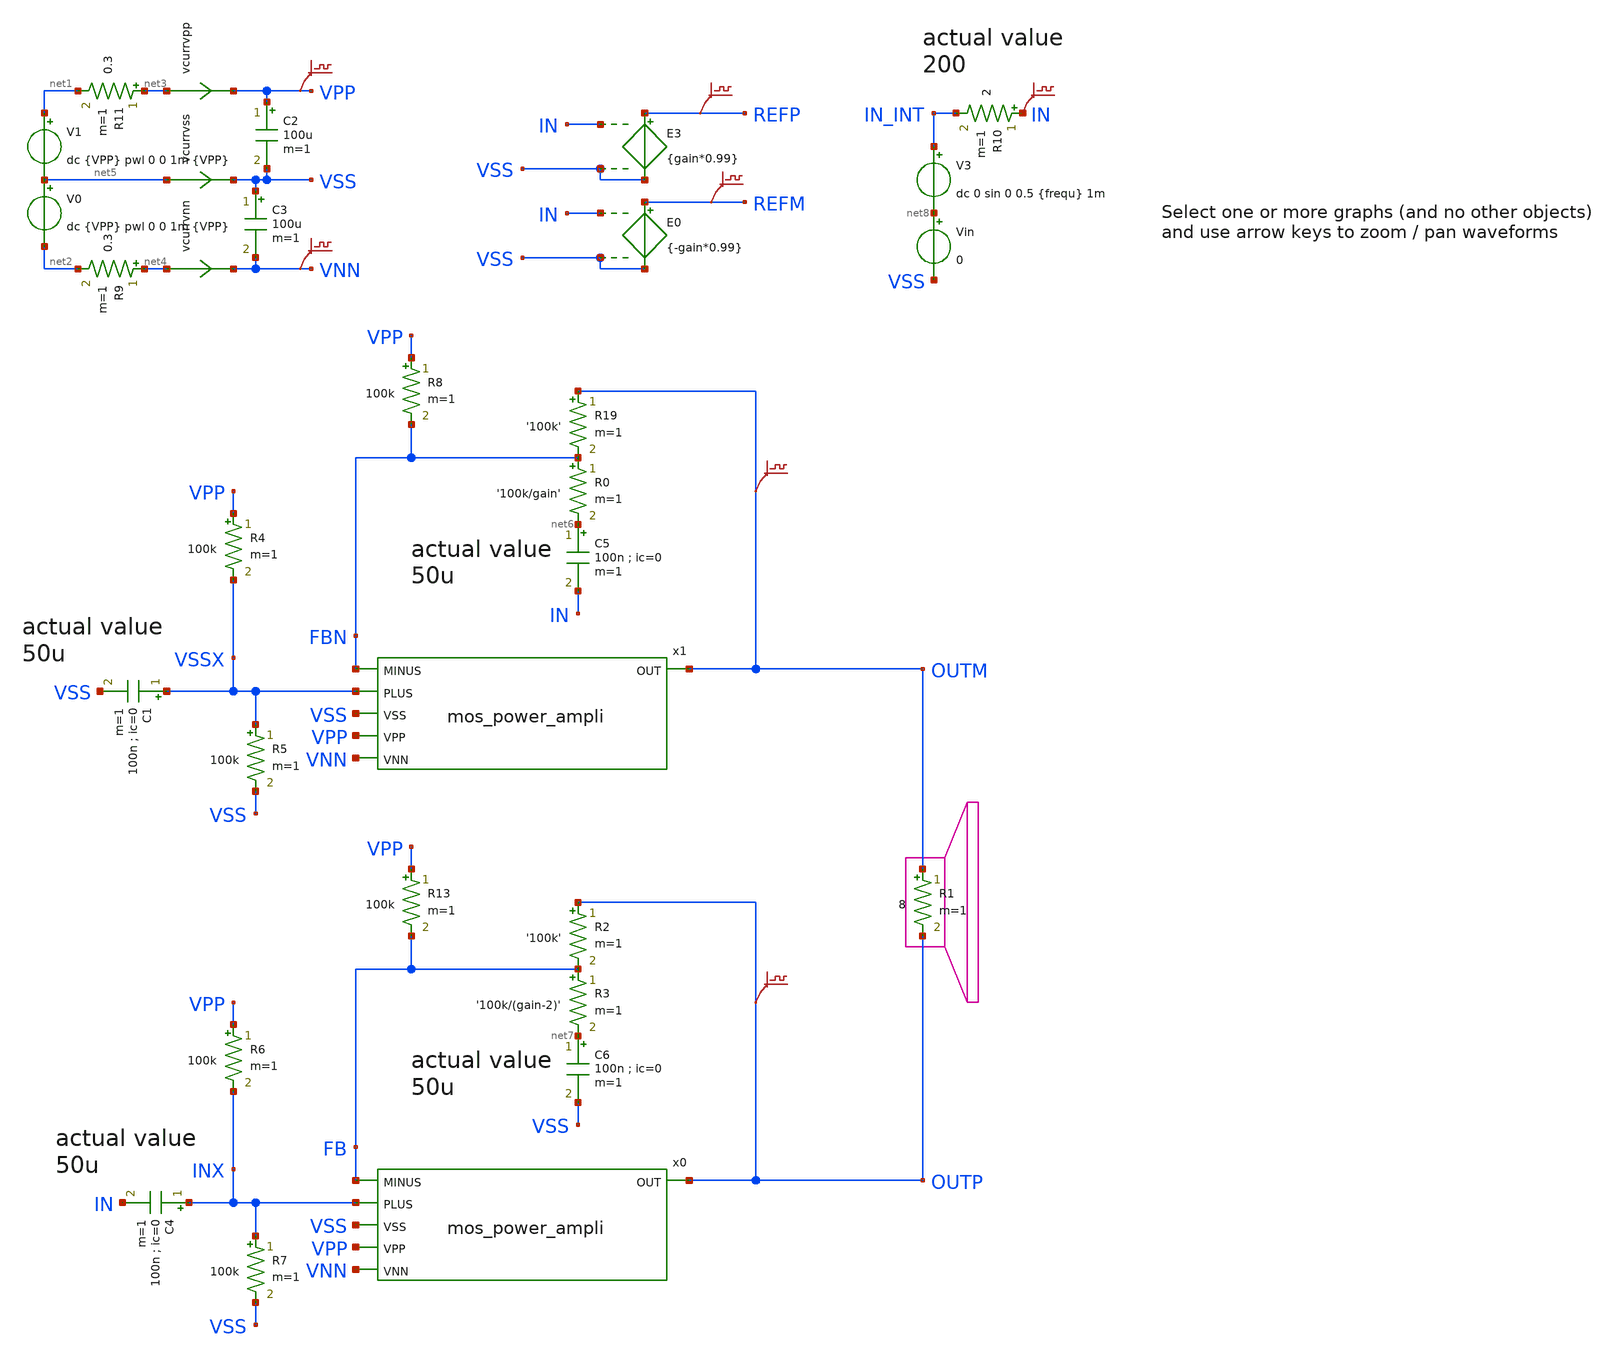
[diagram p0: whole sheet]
** sch_path: xschem_library/examples/poweramp.sch
* Copyright (C) 1998-2023 Stefan Frederik Schippers
* This program is free software; you can redistribute it and/or modify
* it under the terms of the GNU General Public License as published by
* the Free Software Foundation; either version 2 of the License, or
* (at your option) any later version.
* This program is distributed in the hope that it will be useful,
* but WITHOUT ANY WARRANTY; without even the implied warranty of
* MERCHANTABILITY or FITNESS FOR A PARTICULAR PURPOSE.  See the
* GNU General Public License for more details.
* You should have received a copy of the GNU General Public License
* along with this program; if not, write to the Free Software
**.subckt poweramp
V1 net1 net5 dc {VPP} pwl 0 0 1m {VPP}
V0 net5 net2 dc {VPP} pwl 0 0 1m {VPP}
R1 OUTM OUTP 8 m=1
E3 REFP VSS IN VSS {gain*0.99}
C3 VSS VNN 100u m=1
R11 net3 net1 0.3 m=1
R9 net4 net2 0.3 m=1
R19 OUTM FBN '100k' m=1
R0 FBN net6 '100k/gain' m=1
x1 FBN VSSX VSS OUTM VPP VNN mos_power_ampli
x0 FB INX VSS OUTP VPP VNN mos_power_ampli
R6 VPP INX 100k m=1
R7 INX VSS 100k m=1
E0 REFM VSS IN VSS {-gain*0.99}
C5 net6 IN 100n ; ic=0 m=1
C6 net7 VSS 100n ; ic=0 m=1
R2 OUTP FB '100k' m=1
R3 FB net7 '100k/(gain-2)' m=1
V3 IN_INT net8 dc 0 sin 0 0.5 {frequ} 1m
R4 VPP VSSX 100k m=1
R5 VSSX VSS 100k m=1
R8 VPP FBN 100k m=1
C4 INX IN 100n ; ic=0 m=1
C1 VSSX VSS 100n ; ic=0 m=1
R10 IN IN_INT 2 m=1
R13 VPP FB 100k m=1
Vin net8 VSS 0
vcurrvpp net3 VPP 0
.save i(vcurrvpp)
vcurrvnn net4 VNN 0
.save i(vcurrvnn)
vcurrvss net5 VSS 0
.save i(vcurrvss)
C2 VPP VSS 100u m=1
.save v(outm)
.save v(outp)
.save v(refp)
.save v(refm)
.save v(in)
.save v(vpp)
.save v(vnn)
**** begin user architecture code



.option ITL4=20000 ITL5=0
vvss vss 0 dc 0
.temp 27
.param VPP=50
.param frequ=5k
.param gain=45
.option savecurrents

** models are generally not free: you must download
** SPICE models for active devices and put them  into the below
** referenced file in simulation directory.
.include "models_poweramp.txt"
.control
save all
op
write poweramp_op.raw
tran  8e-7 0.025 uic
* .FOUR 20k v(outm,outp)
* .probe i(*)
save p(r*) p(v*)
write poweramp.raw

alterparam VPP=30
reset

save all
op
write poweramp_op2.raw
tran  8e-7 0.025 uic
* .FOUR 20k v(outm,outp)
* .probe i(*)
save p(r*) p(v*)
write poweramp2.raw




quit 0


.endc






**** end user architecture code
**.ends

* expanding   symbol:  mos_power_ampli.sym # of pins=6
** sym_path: xschem_library/examples/mos_power_ampli.sym
** sch_path: xschem_library/examples/mos_power_ampli.sch
.subckt mos_power_ampli MINUS PLUS VSS OUT VPP VNN
*.ipin PLUS
*.ipin VNN
*.opin OUT
*.ipin MINUS
*.ipin VSS
*.ipin VPP
xm2 net1 GB SB irf540 m=1
R7 GB SB 190 m=1
xm1 VPP GA SA irf540 m=1
R0 GA SA 190 m=1
R2 VPP E2 50 m=1
R3 VBOOST E1 50 m=1
Q5 C5 PLUS E9 q2n2222 area=1 m=1
Q4 net9 net2 E4 q2n2907p area=1 m=1
R9 VBOOST E4 50 m=1
Q6 C6 C2 net5 q2n2907p area=1 m=1
R4 VPP E6 50 m=1
vd OUTI net1 0
.save i(vd)
vu SA OUTI 0
.save i(vu)
Q1 net2 net2 E1 q2n2907p area=1 m=1
Q2 C2 C2 net4 q2n2907p area=1 m=1
Q9 C9 MINUS E9 q2n2222 area=1 m=1
R11 GB net6 1300 m=1
Q8 C8 VSS E8 q2n2907p area=1 m=1
C12 VBOOST net3 40u m=1
D0 VPP VBOOST d1n4148 area=1
R18 net3 OUTI 200 m=1
D1 VPP VBOOST d1n758
R14 B1 net7 4k m=1
Q11 GA B1 E11 q2n2907p area=1 m=1
R15 VBOOST B1 4k m=1
R5 E9 net10 120 m=1
R6 net10 net11 120 m=1
D2 VSS B3 d1n755
Q3 C3 B3 E3 q2n2222 area=1 m=1
R1 VPP B3 10k m=1
R10 E3 VSS 170 m=1
C3 B3 VSS 100n m=1
R12 C6 E8 1300 m=1
R13 C2 C9 300 m=1
Q7 C7 net8 C5 q2n2222 area=1 m=1
v0 SB VNN 0
.save i(v0)
v1 E6 net5 0
.save i(v1)
v2 E2 net4 0
.save i(v2)
v3 net11 C3 0
.save i(v3)
v4 C8 net6 0
.save i(v4)
v5 net7 OUTI 0
.save i(v5)
v6 net2 C7 0
.save i(v6)
v7 net9 E11 0
.save i(v7)
.save v(gb)
.save v(sb)
.save v(ga)
.save v(sa)
v8 OUTI OUT 0
.save i(v8)
.save v(ga)
.save v(gb)
.save v(c2)
.save v(net2)
.save v(c7)
.save v(vboost)
.save v(outi)
v9 C9 net8 0
.save i(v9)
.ends

.end
